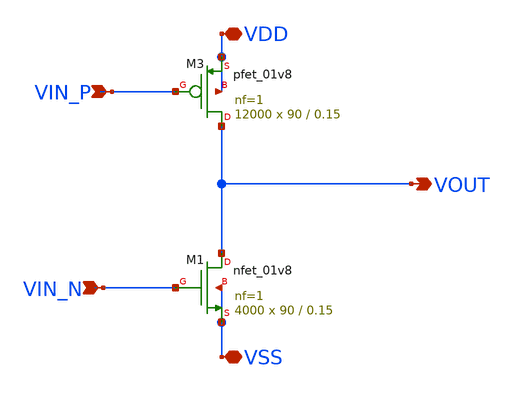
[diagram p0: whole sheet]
** sch_path: xschem/DC_DC_Converter_xschem/OTHERS/DC_DC_Converter_3/Inverter_5/Inverter5.sch
**.subckt Inverter5 VIN_N VDD VSS VOUT VIN_P
*.ipin VIN_N
*.iopin VDD
*.iopin VSS
*.opin VOUT
*.ipin VIN_P
XM1 VOUT VIN_N VSS VSS sky130_fd_pr__nfet_01v8 L=0.15 W=90 nf=1 ad='int((nf+1)/2) * W/nf * 0.29' as='int((nf+2)/2) * W/nf * 0.29'
+ pd='2*int((nf+1)/2) * (W/nf + 0.29)' ps='2*int((nf+2)/2) * (W/nf + 0.29)' nrd='0.29 / W' nrs='0.29 / W'
+ sa=0 sb=0 sd=0 mult=4000 m=4000
XM3 VOUT VIN_P VDD VDD sky130_fd_pr__pfet_01v8 L=0.15 W=90 nf=1 ad='int((nf+1)/2) * W/nf * 0.29' as='int((nf+2)/2) * W/nf * 0.29'
+ pd='2*int((nf+1)/2) * (W/nf + 0.29)' ps='2*int((nf+2)/2) * (W/nf + 0.29)' nrd='0.29 / W' nrs='0.29 / W'
+ sa=0 sb=0 sd=0 mult=12000 m=12000
**.ends
.end
